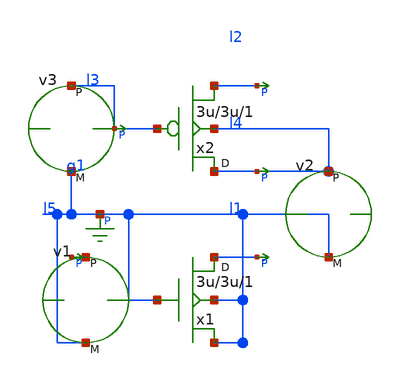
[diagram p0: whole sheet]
** sch_path: common/tests/xschem/cnm25_nmos.sch
**.subckt cnm25_nmos
x1 in 0 0 0 cnm25modN w=3u l=3u m=1
x2 vdd out in vdd cnm25modP w=3u l=3u m=1
v1 in 0 0
v2 vdd 0 5
v3 out 0 5
**.ends
.end
